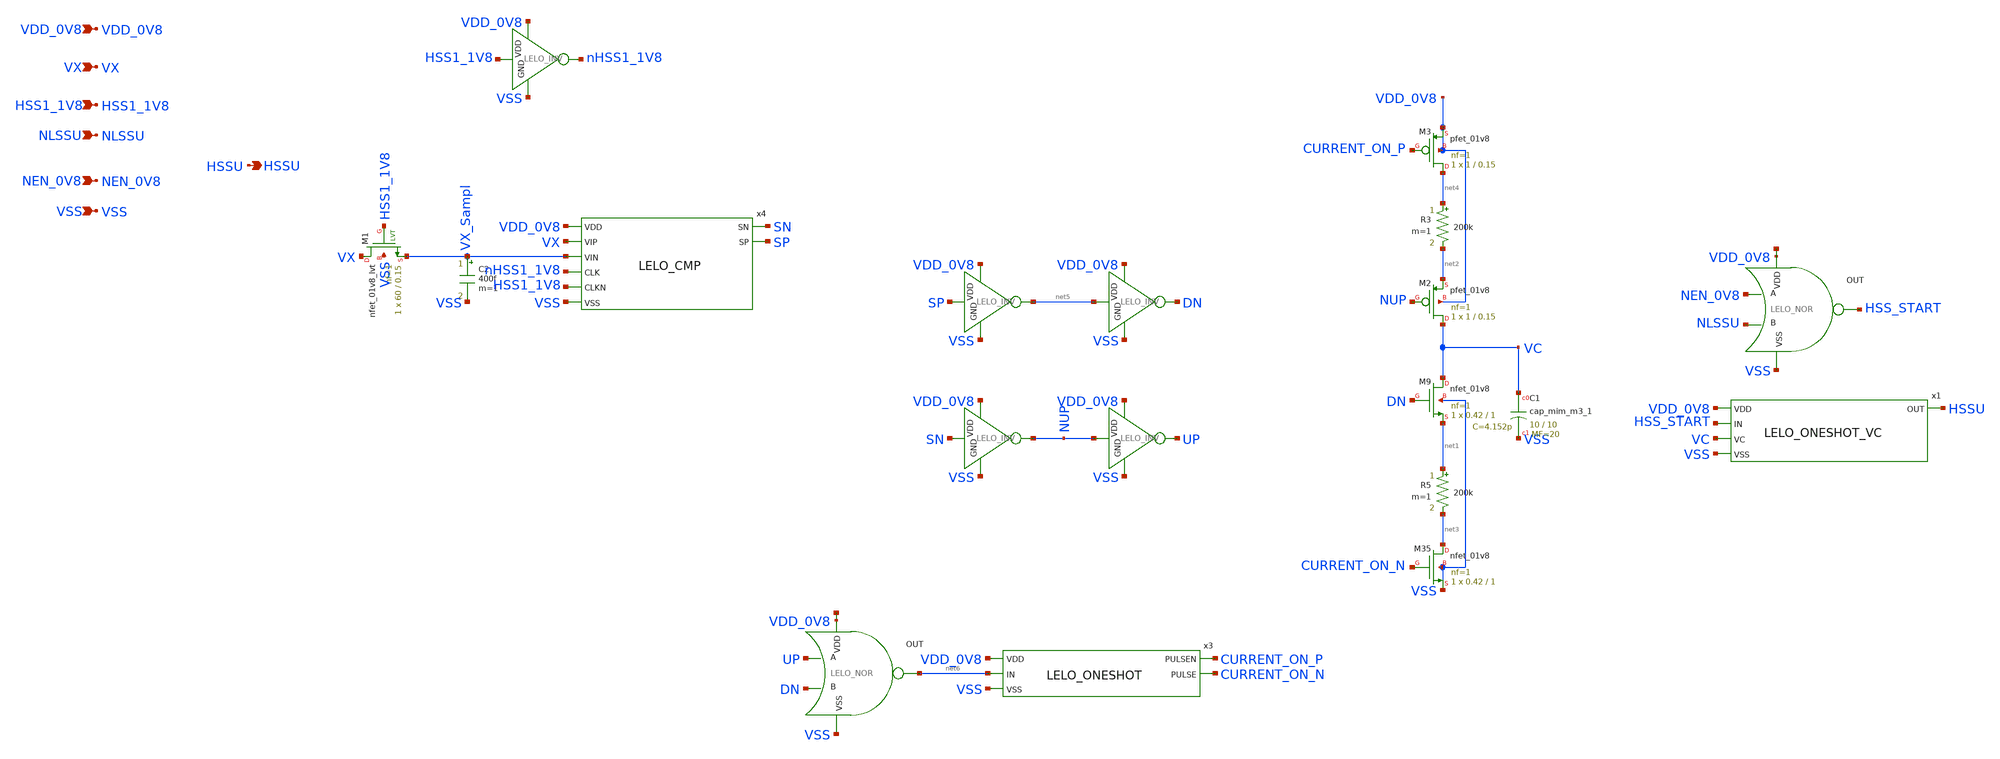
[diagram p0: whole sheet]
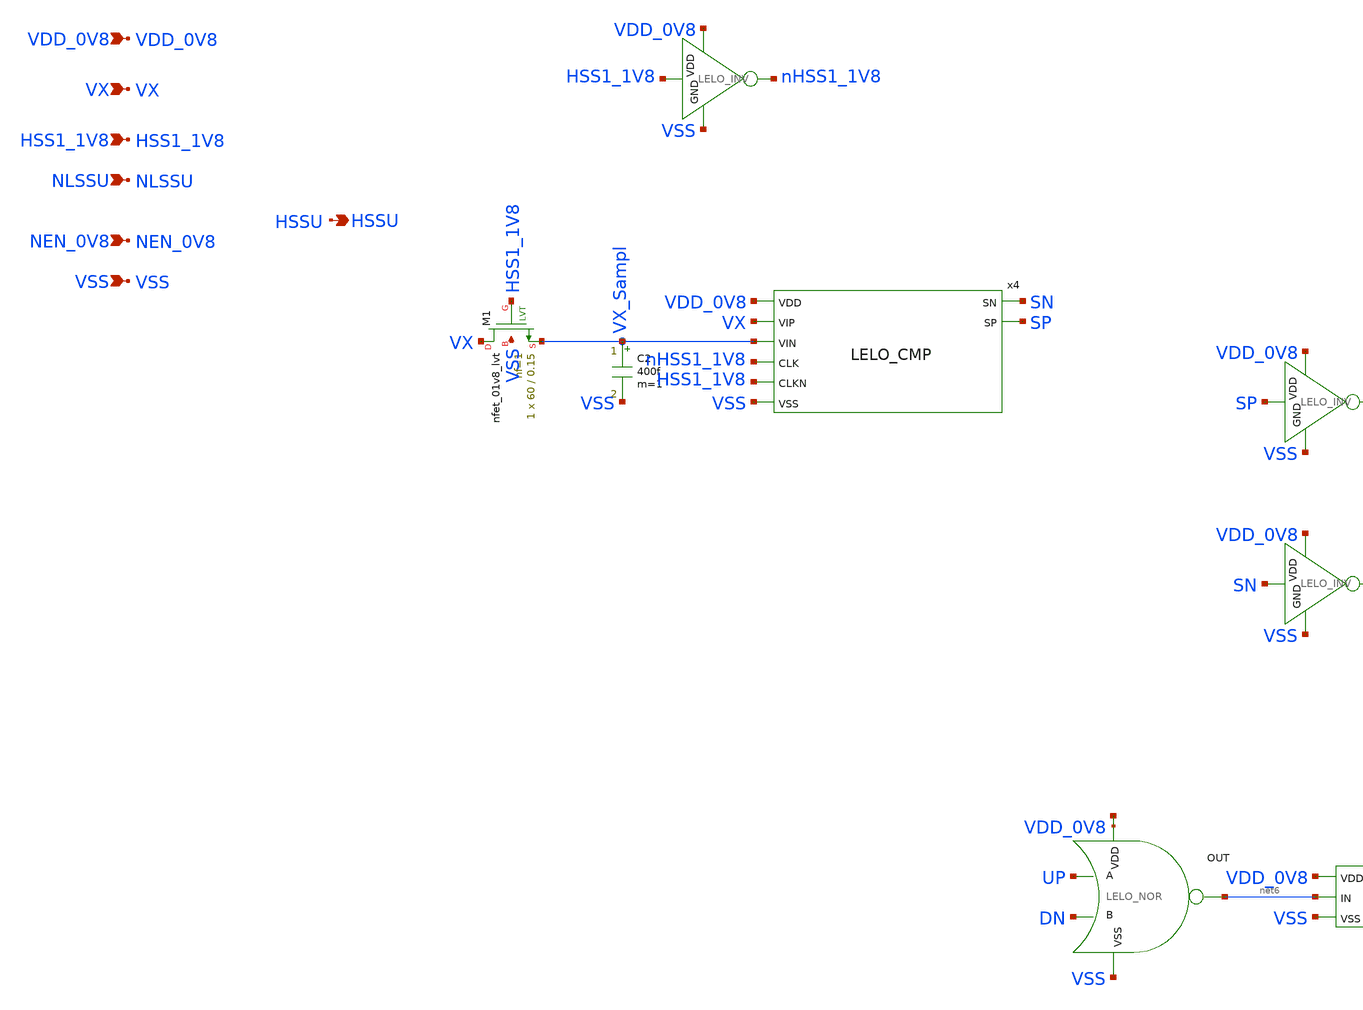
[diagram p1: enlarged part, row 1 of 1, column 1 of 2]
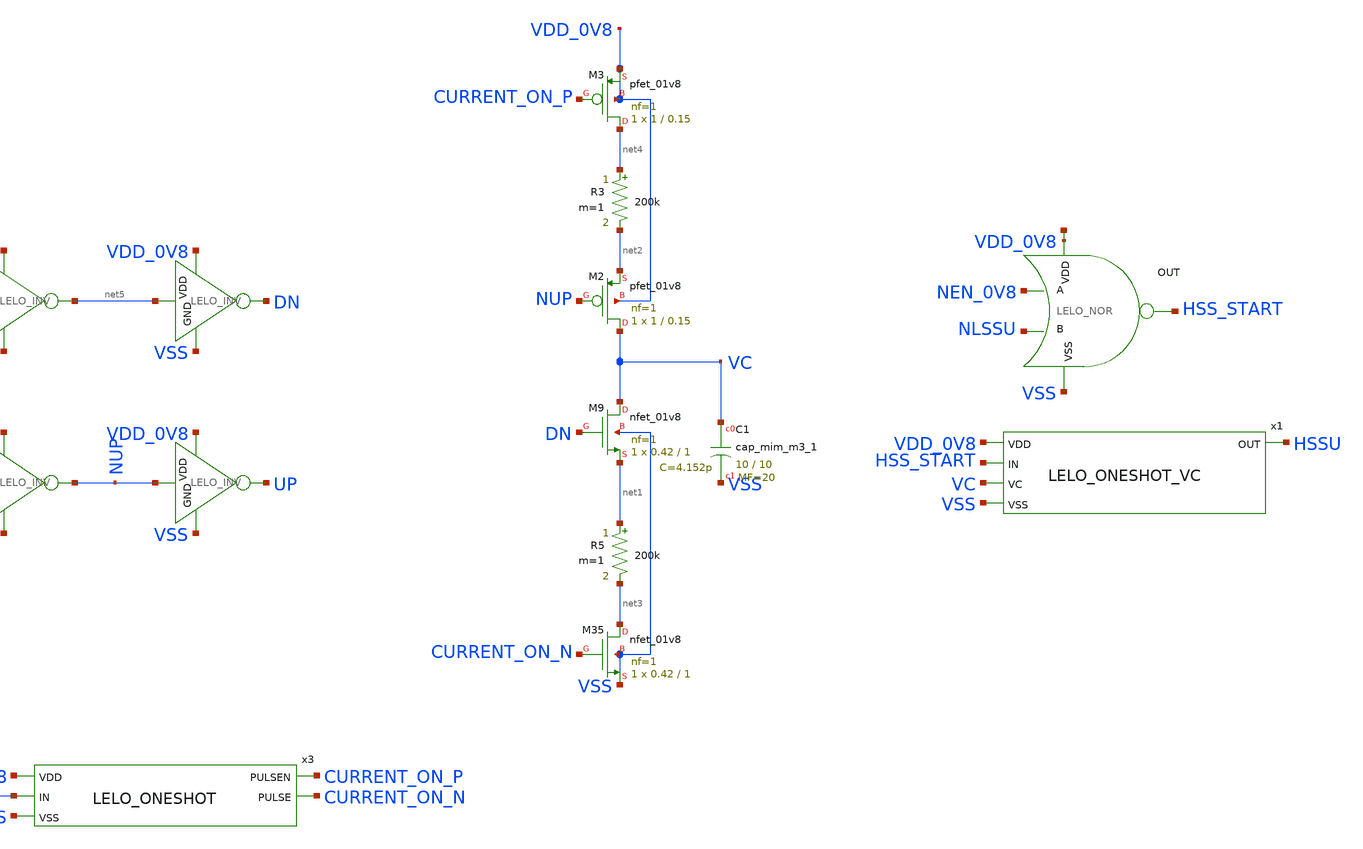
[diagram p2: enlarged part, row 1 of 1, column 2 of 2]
** sch_path: design/LELO_SVOD_SKY130A/LELO_SVOD_HSSCNTRL.sch
**.subckt LELO_SVOD_HSSCNTRL HSSU VX NLSSU VSS NEN_0V8 HSS1_1V8 VDD_0V8
*.opin HSSU
*.ipin VX
*.ipin NLSSU
*.ipin VSS
*.ipin NEN_0V8
*.ipin HSS1_1V8
*.ipin VDD_0V8
x4 SN SP VDD_0V8 VX VX_Sampl nHSS1_1V8 HSS1_1V8 VSS LELO_CMP
XM9 VC DN net1 VSS sky130_fd_pr__nfet_01v8 L=1 W=0.42 nf=1 ad='int((1 + 1)/2) * 0.42 / 1 * 0.29' as='int((1 + 2)/2) * 0.42 / 1 * 0.29'
+ pd='2*int((1 + 1)/2) * (0.42 / 1 + 0.29)' ps='2*int((1 + 2)/2) * (0.42 / 1 + 0.29)' nrd='0.29 / 0.42 '
+ nrs='0.29 / 0.42 ' sa=0 sb=0 sd=0 mult=1 m=1
x10 VDD_0V8 SP net5 VSS LELO_INV
R5 net1 net3 200k m=1
XM35 net3 CURRENT_ON_N VSS VSS sky130_fd_pr__nfet_01v8 L=1 W=0.42 nf=1 ad='int((1 + 1)/2) * 0.42 / 1 * 0.29'
+ as='int((1 + 2)/2) * 0.42 / 1 * 0.29' pd='2*int((1 + 1)/2) * (0.42 / 1 + 0.29)' ps='2*int((1 + 2)/2) * (0.42 / 1 + 0.29)'
+ nrd='0.29 / 0.42 ' nrs='0.29 / 0.42 ' sa=0 sb=0 sd=0 mult=1 m=1
x11 VDD_0V8 SN NUP VSS LELO_INV
x14 VDD_0V8 NUP UP VSS LELO_INV
x17 VDD_0V8 net5 DN VSS LELO_INV
x2 net7 net6 UP DN VSS LELO_NOR
x3 VDD_0V8 net6 VSS CURRENT_ON_P CURRENT_ON_N LELO_ONESHOT
R3 net4 net2 200k m=1
x1 VDD_0V8 HSS_START VC HSSU VSS LELO_ONESHOT_VC
XC1 VC VSS sky130_fd_pr__cap_mim_m3_1 W=10 L=10 MF=20 m=20
C2 VX_Sampl VSS 400f m=1
XM1 VX HSS1_1V8 VX_Sampl VSS sky130_fd_pr__nfet_01v8_lvt L=0.15 W=60 nf=1 ad='int((1 + 1)/2) * 60 / 1 * 0.29'
+ as='int((1 + 2)/2) * 60 / 1 * 0.29' pd='2*int((1 + 1)/2) * (60 / 1 + 0.29)' ps='2*int((1 + 2)/2) * (60 / 1 + 0.29)'
+ nrd='0.29 / 60 ' nrs='0.29 / 60 ' sa=0 sb=0 sd=0 mult=1 m=1
x5 VDD_0V8 HSS1_1V8 nHSS1_1V8 VSS LELO_INV
x6 net8 HSS_START NEN_0V8 NLSSU VSS LELO_NOR
XM2 VC NUP net2 VDD_0V8 sky130_fd_pr__pfet_01v8 L=0.15 W=1 nf=1 ad='int((1 + 1)/2) * 1 / 1 * 0.29' as='int((1 + 2)/2) * 1 / 1 * 0.29'
+ pd='2*int((1 + 1)/2) * (1 / 1 + 0.29)' ps='2*int((1 + 2)/2) * (1 / 1 + 0.29)' nrd='0.29 / 1 ' nrs='0.29 / 1 '
+ sa=0 sb=0 sd=0 mult=1 m=1
XM3 net4 CURRENT_ON_P VDD_0V8 VDD_0V8 sky130_fd_pr__pfet_01v8 L=0.15 W=1 nf=1 ad='int((1 + 1)/2) * 1 / 1 * 0.29'
+ as='int((1 + 2)/2) * 1 / 1 * 0.29' pd='2*int((1 + 1)/2) * (1 / 1 + 0.29)' ps='2*int((1 + 2)/2) * (1 / 1 + 0.29)'
+ nrd='0.29 / 1 ' nrs='0.29 / 1 ' sa=0 sb=0 sd=0 mult=1 m=1
**.ends
.end
